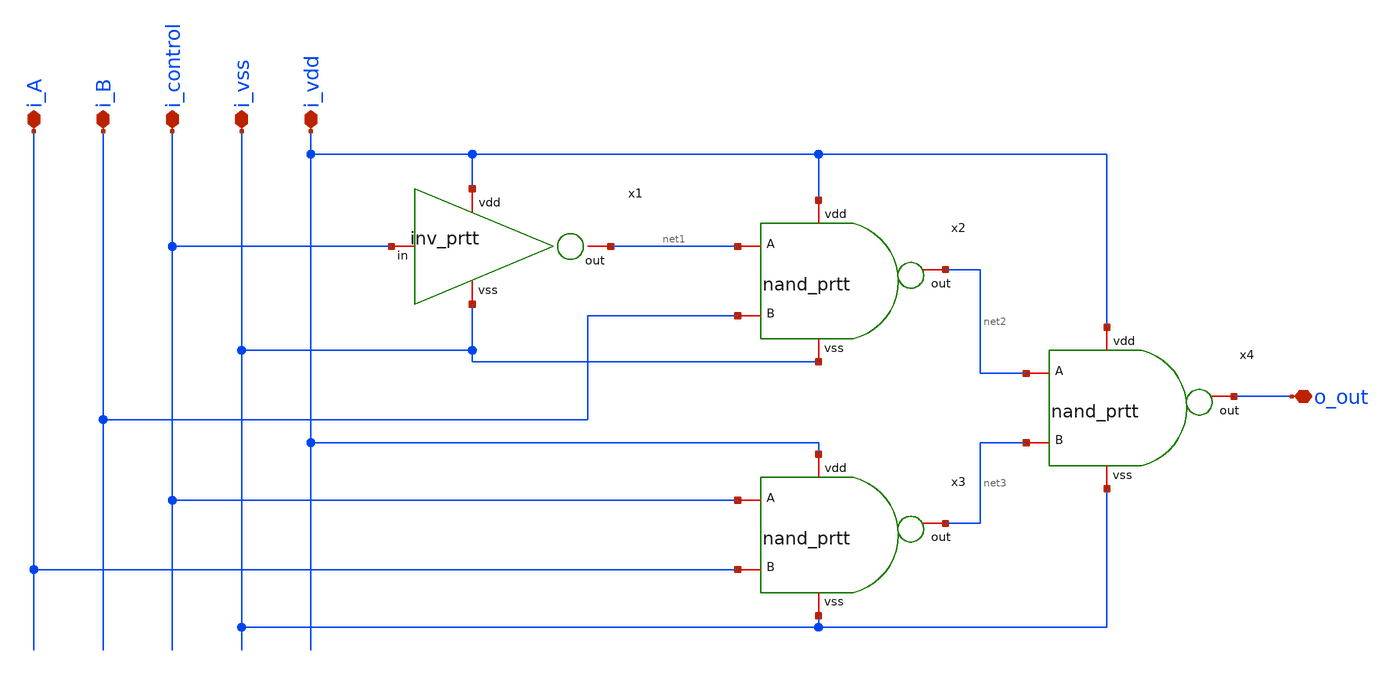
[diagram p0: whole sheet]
** sch_path: PhaseInterpolator/BinarytoThermo/mux.sch
**.subckt mux i_control i_B i_A i_vss i_vdd o_out
*.iopin i_control
*.iopin i_B
*.iopin i_A
*.iopin i_vss
*.iopin i_vdd
*.iopin o_out
x1 i_vdd i_control net1 i_vss inv_prtt
x2 i_vdd net2 net1 i_B i_vss nand_prtt
x3 i_vdd net3 i_control i_A i_vss nand_prtt
x4 i_vdd o_out net2 net3 i_vss nand_prtt
**.ends
.end
